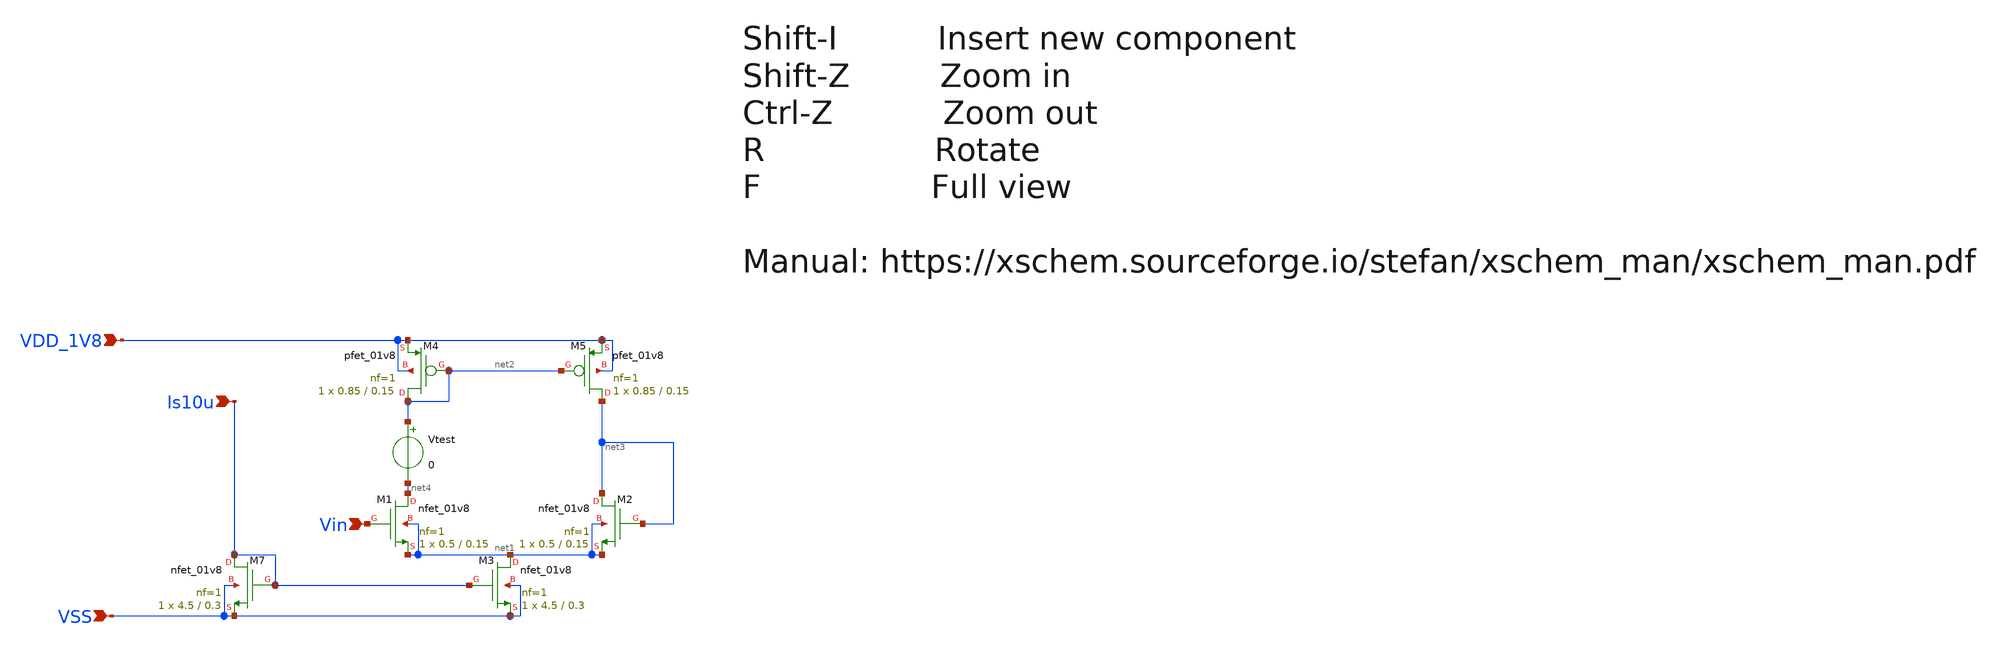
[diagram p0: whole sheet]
** sch_path: design/CNR_GR05_SKY130NM/CNR_GR05.sch
**.subckt CNR_GR05 VDD_1V8 VSS Is10u Vin
*.ipin VDD_1V8
*.ipin VSS
*.ipin Is10u
*.ipin Vin
XM1 net4 Vin net1 net1 sky130_fd_pr__nfet_01v8 L=0.15 W=0.5 nf=1 ad='int((nf+1)/2) * W/nf * 0.29' as='int((nf+2)/2) * W/nf * 0.29'
+ pd='2*int((nf+1)/2) * (W/nf + 0.29)' ps='2*int((nf+2)/2) * (W/nf + 0.29)' nrd='0.29 / W' nrs='0.29 / W'
+ sa=0 sb=0 sd=0 mult=1 m=1
XM2 net3 net3 net1 net1 sky130_fd_pr__nfet_01v8 L=0.15 W=0.5 nf=1 ad='int((nf+1)/2) * W/nf * 0.29' as='int((nf+2)/2) * W/nf * 0.29'
+ pd='2*int((nf+1)/2) * (W/nf + 0.29)' ps='2*int((nf+2)/2) * (W/nf + 0.29)' nrd='0.29 / W' nrs='0.29 / W'
+ sa=0 sb=0 sd=0 mult=1 m=1
XM3 net1 Is10u VSS VSS sky130_fd_pr__nfet_01v8 L=0.3 W=4.5 nf=1 ad='int((nf+1)/2) * W/nf * 0.29' as='int((nf+2)/2) * W/nf * 0.29'
+ pd='2*int((nf+1)/2) * (W/nf + 0.29)' ps='2*int((nf+2)/2) * (W/nf + 0.29)' nrd='0.29 / W' nrs='0.29 / W'
+ sa=0 sb=0 sd=0 mult=1 m=1
XM4 net2 net2 VDD_1V8 VDD_1V8 sky130_fd_pr__pfet_01v8 L=0.15 W=0.85 nf=1 ad='int((nf+1)/2) * W/nf * 0.29'
+ as='int((nf+2)/2) * W/nf * 0.29' pd='2*int((nf+1)/2) * (W/nf + 0.29)' ps='2*int((nf+2)/2) * (W/nf + 0.29)'
+ nrd='0.29 / W' nrs='0.29 / W' sa=0 sb=0 sd=0 mult=1 m=1
XM5 net3 net2 VDD_1V8 VDD_1V8 sky130_fd_pr__pfet_01v8 L=0.15 W=0.85 nf=1 ad='int((nf+1)/2) * W/nf * 0.29'
+ as='int((nf+2)/2) * W/nf * 0.29' pd='2*int((nf+1)/2) * (W/nf + 0.29)' ps='2*int((nf+2)/2) * (W/nf + 0.29)'
+ nrd='0.29 / W' nrs='0.29 / W' sa=0 sb=0 sd=0 mult=1 m=1
XM7 Is10u Is10u VSS VSS sky130_fd_pr__nfet_01v8 L=0.3 W=4.5 nf=1 ad='int((nf+1)/2) * W/nf * 0.29' as='int((nf+2)/2) * W/nf * 0.29'
+ pd='2*int((nf+1)/2) * (W/nf + 0.29)' ps='2*int((nf+2)/2) * (W/nf + 0.29)' nrd='0.29 / W' nrs='0.29 / W'
+ sa=0 sb=0 sd=0 mult=1 m=1
Vtest net2 net4 0
**.ends
.end
